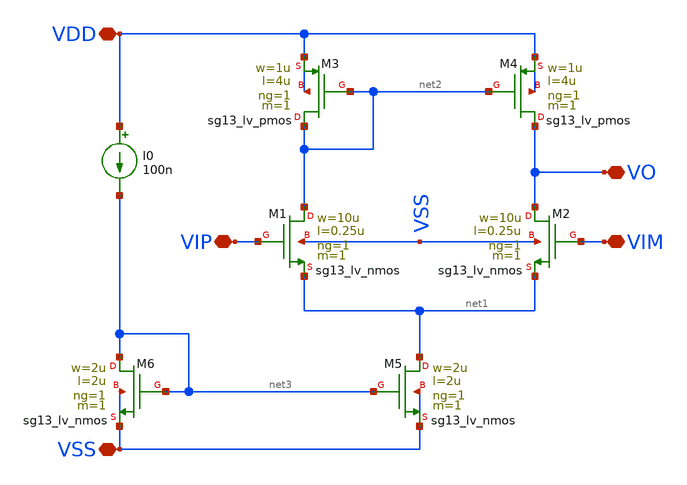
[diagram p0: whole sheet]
** sch_path: analog/core/opamp_01.sch
**.subckt opamp_01 VIM VIP VSS VDD VO
*.iopin VIM
*.iopin VIP
*.iopin VSS
*.iopin VDD
*.iopin VO
XM1 net2 VIP net1 VSS sg13_lv_nmos w=10u l=0.25u ng=1 m=1 mm_ok=1
XM2 VO VIM net1 VSS sg13_lv_nmos w=10u l=0.25u ng=1 m=1 mm_ok=1
XM3 net2 net2 VDD VDD sg13_lv_pmos w=1u l=4u ng=1 m=1 mm_ok=1
XM4 VO net2 VDD VDD sg13_lv_pmos w=1u l=4u ng=1 m=1 mm_ok=1
XM5 net1 net3 VSS VSS sg13_lv_nmos w=2u l=2u ng=1 m=1 mm_ok=1
XM6 net3 net3 VSS VSS sg13_lv_nmos w=2u l=2u ng=1 m=1 mm_ok=1
I0 VDD net3 100n
**.ends
.end
